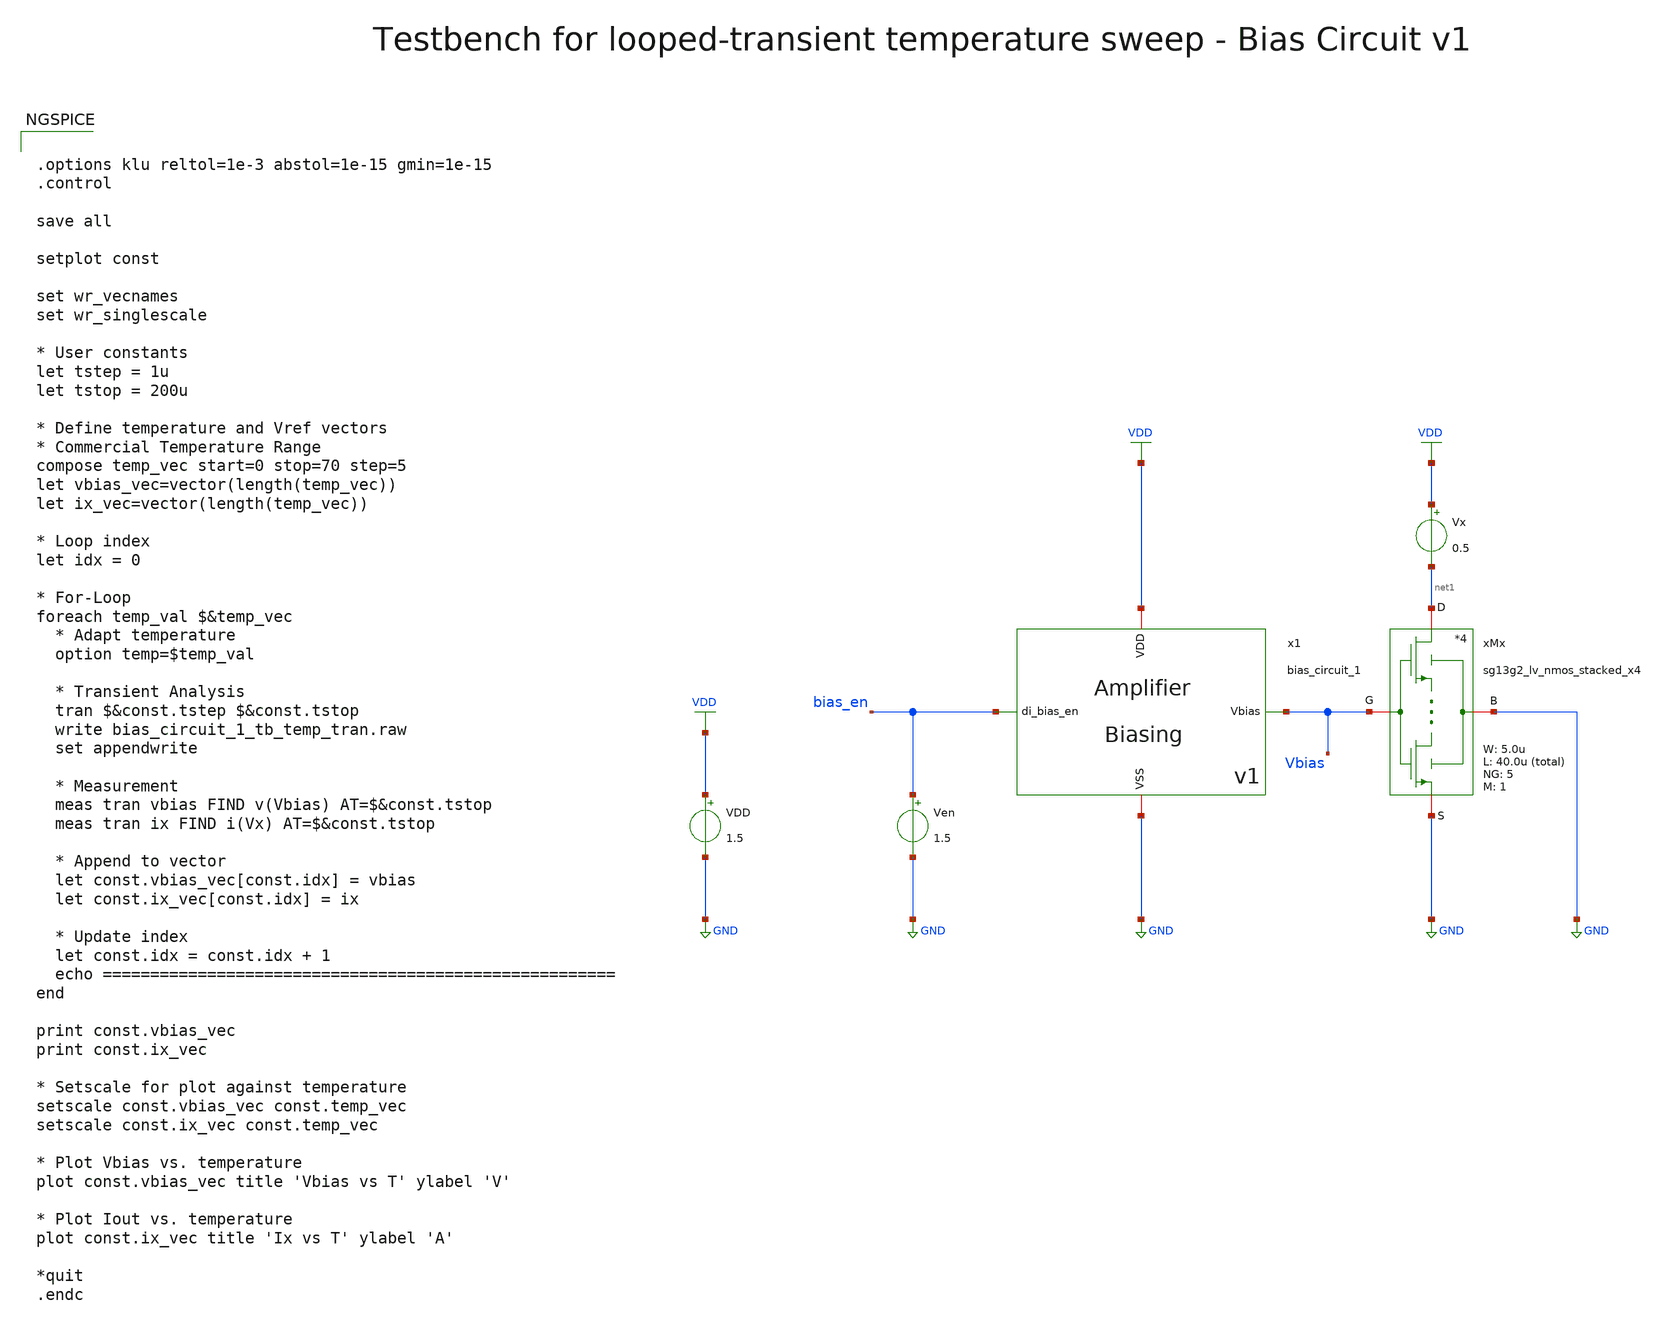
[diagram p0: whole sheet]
** sch_path: SG13G2_ATBS-ADC-main/xschem/bio_amplifier/amplifier_core/bias_circuit/bias_circuit_1/testbenches/bias_circuit_1_tb_temp_tran.sch
**.subckt bias_circuit_1_tb_temp_tran
Ven bias_en GND 1.5
VDD VDD GND 1.5
x1 bias_en Vbias VDD GND bias_circuit_1
xMx net1 Vbias GND GND sg13g2_lv_nmos_stacked_x4 W_N=5.0u L_N=40.0u NG_N=5 M_N=1
Vx VDD net1 0.5
**** begin user architecture code

.lib cornerMOSlv.lib mos_tt
.lib cornerRES.lib res_typ



.options klu reltol=1e-3 abstol=1e-15 gmin=1e-15
.control

save all

setplot const

set wr_vecnames
set wr_singlescale

* User constants
let tstep = 1u
let tstop = 200u

* Define temperature and Vref vectors
* Commercial Temperature Range
compose temp_vec start=0 stop=70 step=5
let vbias_vec=vector(length(temp_vec))
let ix_vec=vector(length(temp_vec))

* Loop index
let idx = 0

* For-Loop
foreach temp_val $&temp_vec
  * Adapt temperature
  option temp=$temp_val

  * Transient Analysis
  tran $&const.tstep $&const.tstop
  write bias_circuit_1_tb_temp_tran.raw
  set appendwrite

  * Measurement
  meas tran vbias FIND v(Vbias) AT=$&const.tstop
  meas tran ix FIND i(Vx) AT=$&const.tstop

  * Append to vector
  let const.vbias_vec[const.idx] = vbias
  let const.ix_vec[const.idx] = ix

  * Update index
  let const.idx = const.idx + 1
  echo ======================================================
end

print const.vbias_vec
print const.ix_vec

* Setscale for plot against temperature
setscale const.vbias_vec const.temp_vec
setscale const.ix_vec const.temp_vec

* Plot Vbias vs. temperature
plot const.vbias_vec title 'Vbias vs T' ylabel 'V'

* Plot Iout vs. temperature
plot const.ix_vec title 'Ix vs T' ylabel 'A'

*quit
.endc

**** end user architecture code
**.ends
.GLOBAL GND
.GLOBAL VDD
.end
